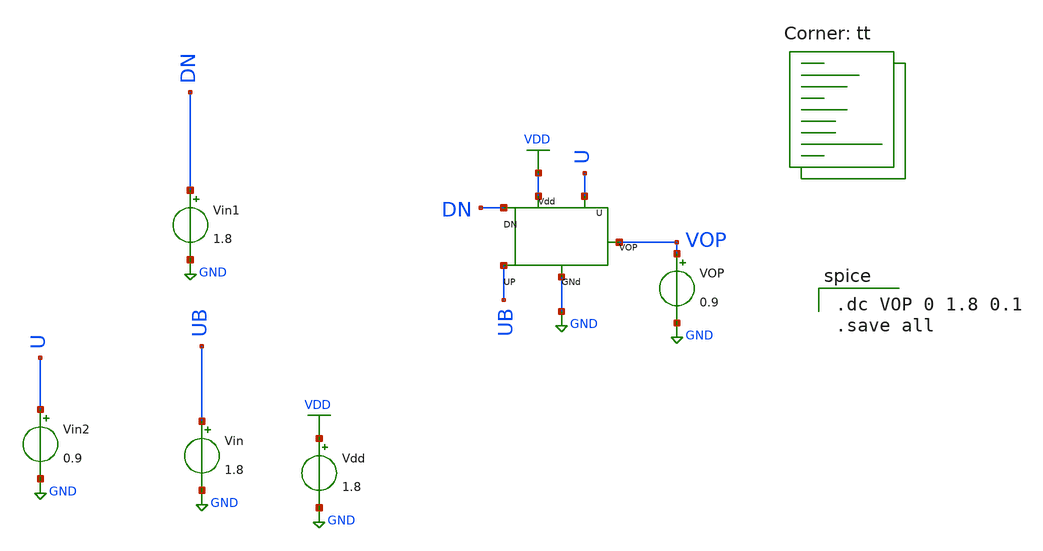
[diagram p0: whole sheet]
** sch_path: pll/pfd_cp_lf_lib/CP_tb/xschem/CP_tb.sch
**.subckt CP_tb
Vdd VDD GND 1.8
Vin UB GND 1.8
Vin1 DN GND 1.8
Vin2 U GND 0.9
X1 DN VOP UB VDD U GND CP
VOP VOP GND 0.9
**** begin user architecture code
.lib $::SKYWATER_MODELS/sky130.lib.spice tt

.dc VOP 0 1.8 0.1
.save all


** opencircuitdesign pdks install
.lib $::SKYWATER_MODELS/sky130.lib.spice tt


**** end user architecture code
**.ends
.GLOBAL GND
.GLOBAL VDD
.end
